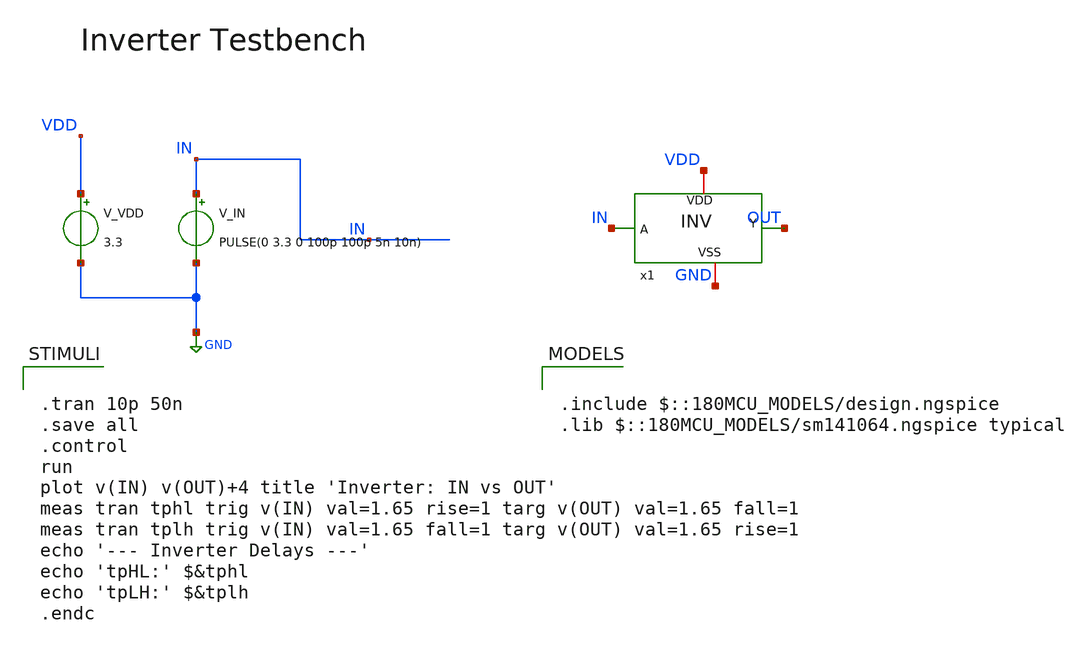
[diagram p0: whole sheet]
** sch_path: designs/libs/core_analog/pfd/leftover_files/inv_tb.sch
**.subckt inv_tb
V_IN IN GND PULSE(0 3.3 0 100p 100p 5n 10n)
V_VDD VDD GND 3.3
x1 VDD OUT IN GND inv
**** begin user architecture code


.tran 10p 50n
.save all
.control
run
plot v(IN) v(OUT)+4 title 'Inverter: IN vs OUT'
meas tran tphl trig v(IN) val=1.65 rise=1 targ v(OUT) val=1.65 fall=1
meas tran tplh trig v(IN) val=1.65 fall=1 targ v(OUT) val=1.65 rise=1
echo '--- Inverter Delays ---'
echo 'tpHL:' $&tphl
echo 'tpLH:' $&tplh
.endc



.include $::180MCU_MODELS/design.ngspice
.lib $::180MCU_MODELS/sm141064.ngspice typical

**** end user architecture code
**.ends
.GLOBAL GND
.end
